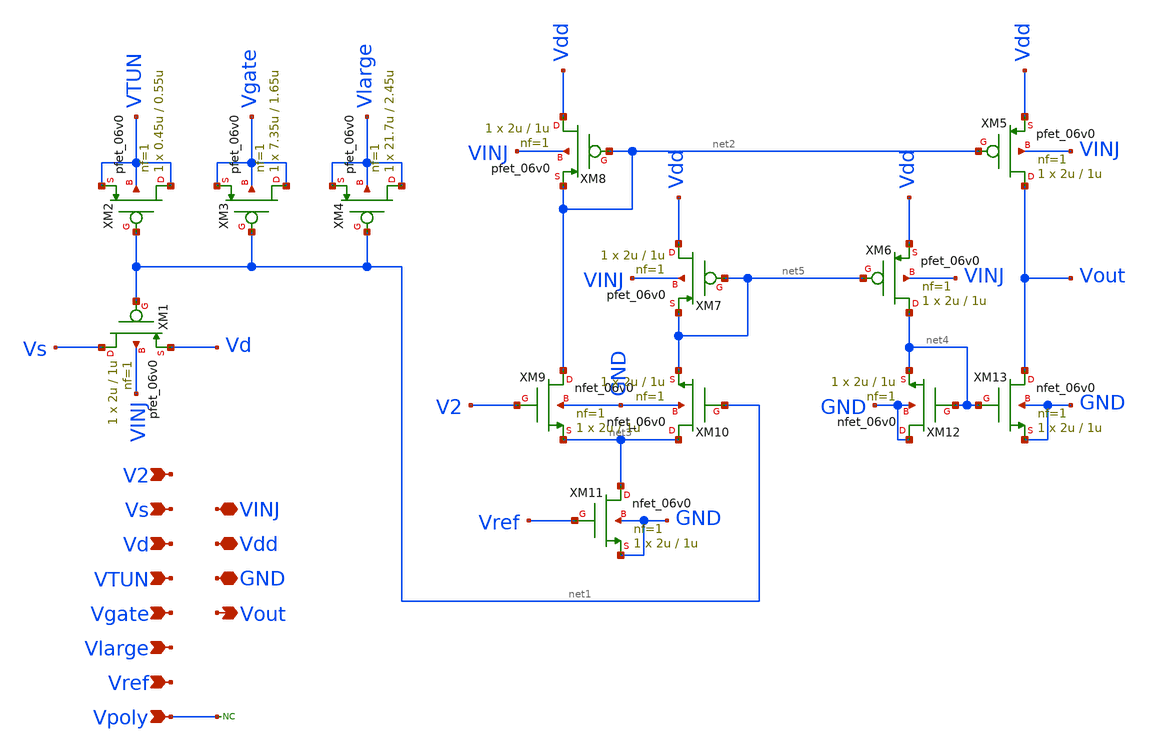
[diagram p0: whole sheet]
** sch_path: 1_Design/GF180_cells/FGCharacterization/gf180_FG_Characterization.sch
**.subckt gf180_FG_Characterization VINJ Vs Vout Vd VTUN Vgate Vlarge Vref Vdd GND Vpoly V2
*.iopin VINJ
*.ipin Vs
*.opin Vout
*.ipin Vd
*.ipin VTUN
*.ipin Vgate
*.ipin Vlarge
*.ipin Vref
*.iopin Vdd
*.iopin GND
*.ipin Vpoly
*.ipin V2
XM1 Vs net1 Vd VINJ pfet_06v0 L=1u W=2u nf=1 ad='int((nf+1)/2) * W/nf * 0.18u' as='int((nf+2)/2) * W/nf * 0.18u'
+ pd='2*int((nf+1)/2) * (W/nf + 0.18u)' ps='2*int((nf+2)/2) * (W/nf + 0.18u)' nrd='0.18u / W' nrs='0.18u / W'
+ sa=0 sb=0 sd=0 m=1
XM2 VTUN net1 VTUN VTUN pfet_06v0 L=0.55u W=0.45u nf=1 ad='int((nf+1)/2) * W/nf * 0.18u' as='int((nf+2)/2) * W/nf * 0.18u'
+ pd='2*int((nf+1)/2) * (W/nf + 0.18u)' ps='2*int((nf+2)/2) * (W/nf + 0.18u)' nrd='0.18u / W' nrs='0.18u / W'
+ sa=0 sb=0 sd=0 m=1
XM3 Vgate net1 Vgate Vgate pfet_06v0 L=1.65u W=7.35u nf=1 ad='int((nf+1)/2) * W/nf * 0.18u' as='int((nf+2)/2) * W/nf * 0.18u'
+ pd='2*int((nf+1)/2) * (W/nf + 0.18u)' ps='2*int((nf+2)/2) * (W/nf + 0.18u)' nrd='0.18u / W' nrs='0.18u / W'
+ sa=0 sb=0 sd=0 m=1
XM4 Vlarge net1 Vlarge Vlarge pfet_06v0 L=2.45u W=21.7u nf=1 ad='int((nf+1)/2) * W/nf * 0.18u' as='int((nf+2)/2) * W/nf * 0.18u'
+ pd='2*int((nf+1)/2) * (W/nf + 0.18u)' ps='2*int((nf+2)/2) * (W/nf + 0.18u)' nrd='0.18u / W' nrs='0.18u / W'
+ sa=0 sb=0 sd=0 m=1
XM5 Vout net2 Vdd VINJ pfet_06v0 L=1u W=2u nf=1 ad='int((nf+1)/2) * W/nf * 0.18u' as='int((nf+2)/2) * W/nf * 0.18u'
+ pd='2*int((nf+1)/2) * (W/nf + 0.18u)' ps='2*int((nf+2)/2) * (W/nf + 0.18u)' nrd='0.18u / W' nrs='0.18u / W'
+ sa=0 sb=0 sd=0 m=1
XM6 net4 net5 Vdd VINJ pfet_06v0 L=1u W=2u nf=1 ad='int((nf+1)/2) * W/nf * 0.18u' as='int((nf+2)/2) * W/nf * 0.18u'
+ pd='2*int((nf+1)/2) * (W/nf + 0.18u)' ps='2*int((nf+2)/2) * (W/nf + 0.18u)' nrd='0.18u / W' nrs='0.18u / W'
+ sa=0 sb=0 sd=0 m=1
XM7 Vdd net5 net5 VINJ pfet_06v0 L=1u W=2u nf=1 ad='int((nf+1)/2) * W/nf * 0.18u' as='int((nf+2)/2) * W/nf * 0.18u'
+ pd='2*int((nf+1)/2) * (W/nf + 0.18u)' ps='2*int((nf+2)/2) * (W/nf + 0.18u)' nrd='0.18u / W' nrs='0.18u / W'
+ sa=0 sb=0 sd=0 m=1
XM8 Vdd net2 net2 VINJ pfet_06v0 L=1u W=2u nf=1 ad='int((nf+1)/2) * W/nf * 0.18u' as='int((nf+2)/2) * W/nf * 0.18u'
+ pd='2*int((nf+1)/2) * (W/nf + 0.18u)' ps='2*int((nf+2)/2) * (W/nf + 0.18u)' nrd='0.18u / W' nrs='0.18u / W'
+ sa=0 sb=0 sd=0 m=1
XM9 net2 V2 net3 GND nfet_06v0 L=1u W=2u nf=1 ad='int((nf+1)/2) * W/nf * 0.18u' as='int((nf+2)/2) * W/nf * 0.18u'
+ pd='2*int((nf+1)/2) * (W/nf + 0.18u)' ps='2*int((nf+2)/2) * (W/nf + 0.18u)' nrd='0.18u / W' nrs='0.18u / W'
+ sa=0 sb=0 sd=0 m=1
XM10 net3 net1 net5 GND nfet_06v0 L=1u W=2u nf=1 ad='int((nf+1)/2) * W/nf * 0.18u' as='int((nf+2)/2) * W/nf * 0.18u'
+ pd='2*int((nf+1)/2) * (W/nf + 0.18u)' ps='2*int((nf+2)/2) * (W/nf + 0.18u)' nrd='0.18u / W' nrs='0.18u / W'
+ sa=0 sb=0 sd=0 m=1
XM11 net3 Vref GND GND nfet_06v0 L=1u W=2u nf=1 ad='int((nf+1)/2) * W/nf * 0.18u' as='int((nf+2)/2) * W/nf * 0.18u'
+ pd='2*int((nf+1)/2) * (W/nf + 0.18u)' ps='2*int((nf+2)/2) * (W/nf + 0.18u)' nrd='0.18u / W' nrs='0.18u / W'
+ sa=0 sb=0 sd=0 m=1
XM12 GND net4 net4 GND nfet_06v0 L=1u W=2u nf=1 ad='int((nf+1)/2) * W/nf * 0.18u' as='int((nf+2)/2) * W/nf * 0.18u'
+ pd='2*int((nf+1)/2) * (W/nf + 0.18u)' ps='2*int((nf+2)/2) * (W/nf + 0.18u)' nrd='0.18u / W' nrs='0.18u / W'
+ sa=0 sb=0 sd=0 m=1
XM13 Vout net4 GND GND nfet_06v0 L=1u W=2u nf=1 ad='int((nf+1)/2) * W/nf * 0.18u' as='int((nf+2)/2) * W/nf * 0.18u'
+ pd='2*int((nf+1)/2) * (W/nf + 0.18u)' ps='2*int((nf+2)/2) * (W/nf + 0.18u)' nrd='0.18u / W' nrs='0.18u / W'
+ sa=0 sb=0 sd=0 m=1
* noconn Vpoly
**.ends
.end
